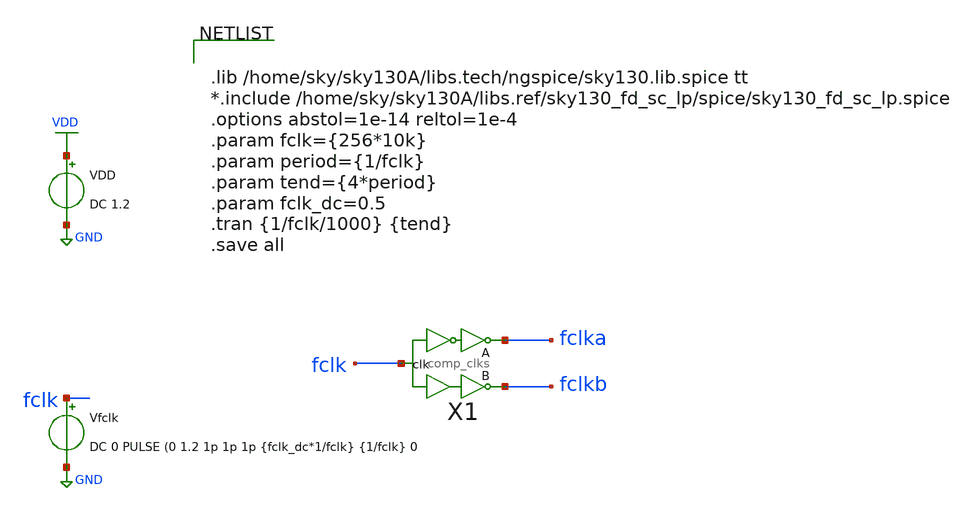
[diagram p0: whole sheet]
** sch_path: xschem/clkgen/comp_clks_tb.sch
**.subckt comp_clks_tb
VDD VDD GND DC 1.2
Vfclk fclk GND DC 0 PULSE (0 1.2 1p 1p 1p {fclk_dc*1/fclk} {1/fclk} 0
X1 fclk fclka fclkb comp_clks Wpmos=1.26 Lpmos=0.18 Wnmos=0.42 Lnmos=0.18
**** begin user architecture code


.lib /home/sky/sky130A/libs.tech/ngspice/sky130.lib.spice tt
*.include /home/sky/sky130A/libs.ref/sky130_fd_sc_lp/spice/sky130_fd_sc_lp.spice
.options abstol=1e-14 reltol=1e-4
.param fclk={256*10k}
.param period={1/fclk}
.param tend={4*period}
.param fclk_dc=0.5
.tran {1/fclk/1000} {tend}
.save all


**** end user architecture code
**.ends

* expanding   symbol:  clkgen/comp_clks.sym # of pins=3
** sym_path: xschem/clkgen/comp_clks.sym
** sch_path: xschem/clkgen/comp_clks.sch
.subckt comp_clks clk clka clkb  Wpmos=3 Lpmos=0.18 Wnmos=1 Lnmos=0.18
*.ipin clk
*.opin clka
*.opin clkb
X3 clk clkt GND VDD transmission_gate Wpmos=Wpmos Lpmos=Lpmos Wnmos=Wnmos Lnmos=Lnmos
X1 clk clki inv Wpmos=3 Lpmos=0.18 Wnmos=1 Lnmos=0.18
X2 clki clka inv Wpmos=3 Lpmos=0.18 Wnmos=1 Lnmos=0.18
X4 clkt clkb inv Wpmos=3 Lpmos=0.18 Wnmos=1 Lnmos=0.18
.ends


* expanding   symbol:  transmission_gate/transmission_gate.sym # of pins=4
** sym_path: xschem/transmission_gate/transmission_gate.sym
** sch_path: xschem/transmission_gate/transmission_gate.sch
.subckt transmission_gate in out ctrl_ ctrl  Wpmos=0.42 Lpmos=0.18 Wnmos=0.42 Lnmos=0.18
*.iopin in
*.iopin out
*.ipin ctrl_
*.ipin ctrl
XM1 out ctrl in GND sky130_fd_pr__nfet_01v8 L=Lnmos W=Wnmos nf=1 ad='int((nf+1)/2) * W/nf * 0.29' as='int((nf+2)/2) * W/nf * 0.29'
+ pd='2*int((nf+1)/2) * (W/nf + 0.29)' ps='2*int((nf+2)/2) * (W/nf + 0.29)' nrd='0.29 / W' nrs='0.29 / W'
+ sa=0 sb=0 sd=0 mult=1 m=1
XM2 out ctrl_ in VDD sky130_fd_pr__pfet_01v8 L=Lpmos W=Wpmos nf=1 ad='int((nf+1)/2) * W/nf * 0.29' as='int((nf+2)/2) * W/nf * 0.29'
+ pd='2*int((nf+1)/2) * (W/nf + 0.29)' ps='2*int((nf+2)/2) * (W/nf + 0.29)' nrd='0.29 / W' nrs='0.29 / W'
+ sa=0 sb=0 sd=0 mult=1 m=1
.ends


* expanding   symbol:  inv/inv.sym # of pins=2
** sym_path: xschem/inv/inv.sym
** sch_path: xschem/inv/inv.sch
.subckt inv in out  Wpmos=3 Lpmos=0.18 Wnmos=1 Lnmos=0.18
*.ipin in
*.iopin out
XM1 out in GND GND sky130_fd_pr__nfet_01v8 L=Lnmos W=Wnmos nf=1 ad='int((nf+1)/2) * W/nf * 0.29' as='int((nf+2)/2) * W/nf * 0.29'
+ pd='2*int((nf+1)/2) * (W/nf + 0.29)' ps='2*int((nf+2)/2) * (W/nf + 0.29)' nrd='0.29 / W' nrs='0.29 / W'
+ sa=0 sb=0 sd=0 mult=1 m=1
XM2 out in VDD VDD sky130_fd_pr__pfet_01v8 L=Lpmos W=Wpmos nf=1 ad='int((nf+1)/2) * W/nf * 0.29' as='int((nf+2)/2) * W/nf * 0.29'
+ pd='2*int((nf+1)/2) * (W/nf + 0.29)' ps='2*int((nf+2)/2) * (W/nf + 0.29)' nrd='0.29 / W' nrs='0.29 / W'
+ sa=0 sb=0 sd=0 mult=1 m=1
.ends

.GLOBAL VDD
.GLOBAL GND
.end
